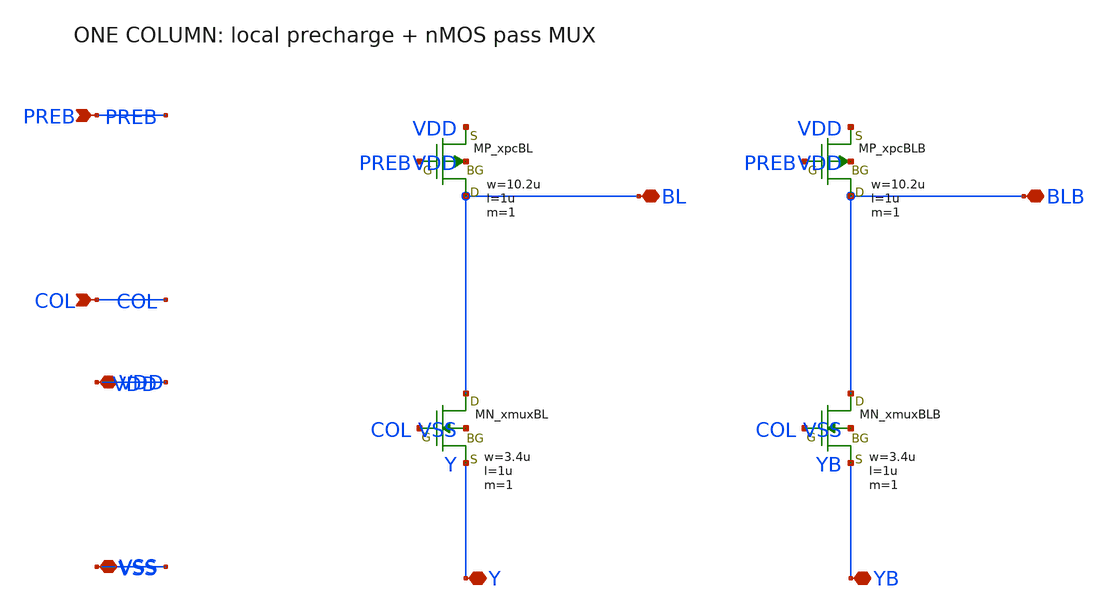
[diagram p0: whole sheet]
** sch_path: sram512_column.sch
**.subckt sram512_column BL Y BLB YB PREB COL VDD VSS
*.iopin BL
*.iopin Y
*.iopin BLB
*.iopin YB
*.ipin PREB
*.ipin COL
*.iopin VDD
*.iopin VSS
XxpcBL BL PREB VDD VDD PMOS w=10.2u l=1u nrd=0 nrs=0 m=1
XxmuxBL BL COL Y VSS NMOS w=3.4u l=1u nrd=0 nrs=0 m=1
XxpcBLB BLB PREB VDD VDD PMOS w=10.2u l=1u nrd=0 nrs=0 m=1
XxmuxBLB BLB COL YB VSS NMOS w=3.4u l=1u nrd=0 nrs=0 m=1
**.ends
.end
